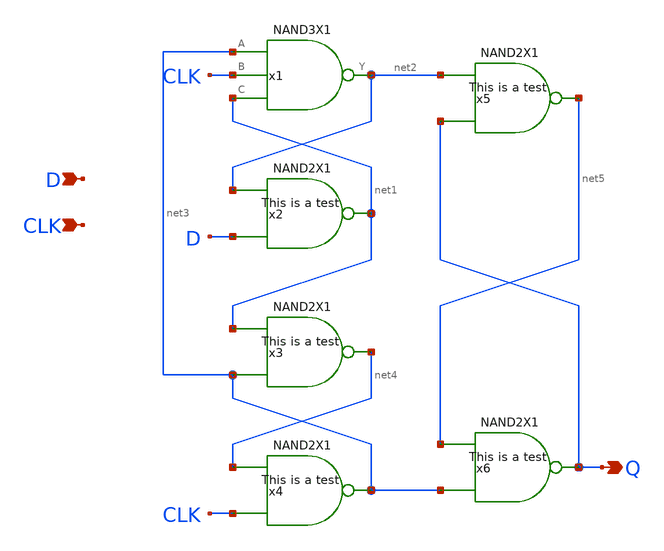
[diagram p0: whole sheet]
** sch_path: lib/xschem/DFFQX1.sch
**.subckt DFFQX1 Q D CLK
*.opin Q
*.ipin D
*.ipin CLK
x1 net2 net3 CLK net1 VDD VSS NAND3X1
x2 net1 net2 D VDD VSS NAND2X1
x3 net4 net1 net3 VDD VSS NAND2X1
x4 net3 net4 CLK VDD VSS NAND2X1
x5 net5 net2 Q VDD VSS NAND2X1
x6 Q net5 net3 VDD VSS NAND2X1
**.ends
.end
